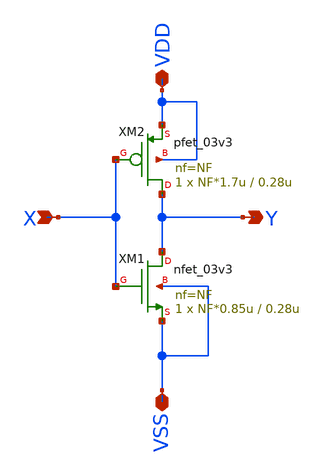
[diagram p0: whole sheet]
** sch_path: xschem_lib/DFFRAM_full_custom/inv.sch
**.subckt inv VSS X Y VDD
*.iopin VSS
*.ipin X
*.opin Y
*.iopin VDD
XM1 Y X VSS VSS nfet_03v3 L=0.28u W=NF*0.85u nf=NF ad='int((nf+1)/2) * W/nf * 0.18u' as='int((nf+2)/2) * W/nf * 0.18u'
+ pd='2*int((nf+1)/2) * (W/nf + 0.18u)' ps='2*int((nf+2)/2) * (W/nf + 0.18u)' nrd='0.18u / W' nrs='0.18u / W'
+ sa=0 sb=0 sd=0 m=1
XM2 Y X VDD VDD pfet_03v3 L=0.28u W=NF*1.7u nf=NF ad='int((nf+1)/2) * W/nf * 0.18u' as='int((nf+2)/2) * W/nf * 0.18u'
+ pd='2*int((nf+1)/2) * (W/nf + 0.18u)' ps='2*int((nf+2)/2) * (W/nf + 0.18u)' nrd='0.18u / W' nrs='0.18u / W'
+ sa=0 sb=0 sd=0 m=1
**.ends
.end
